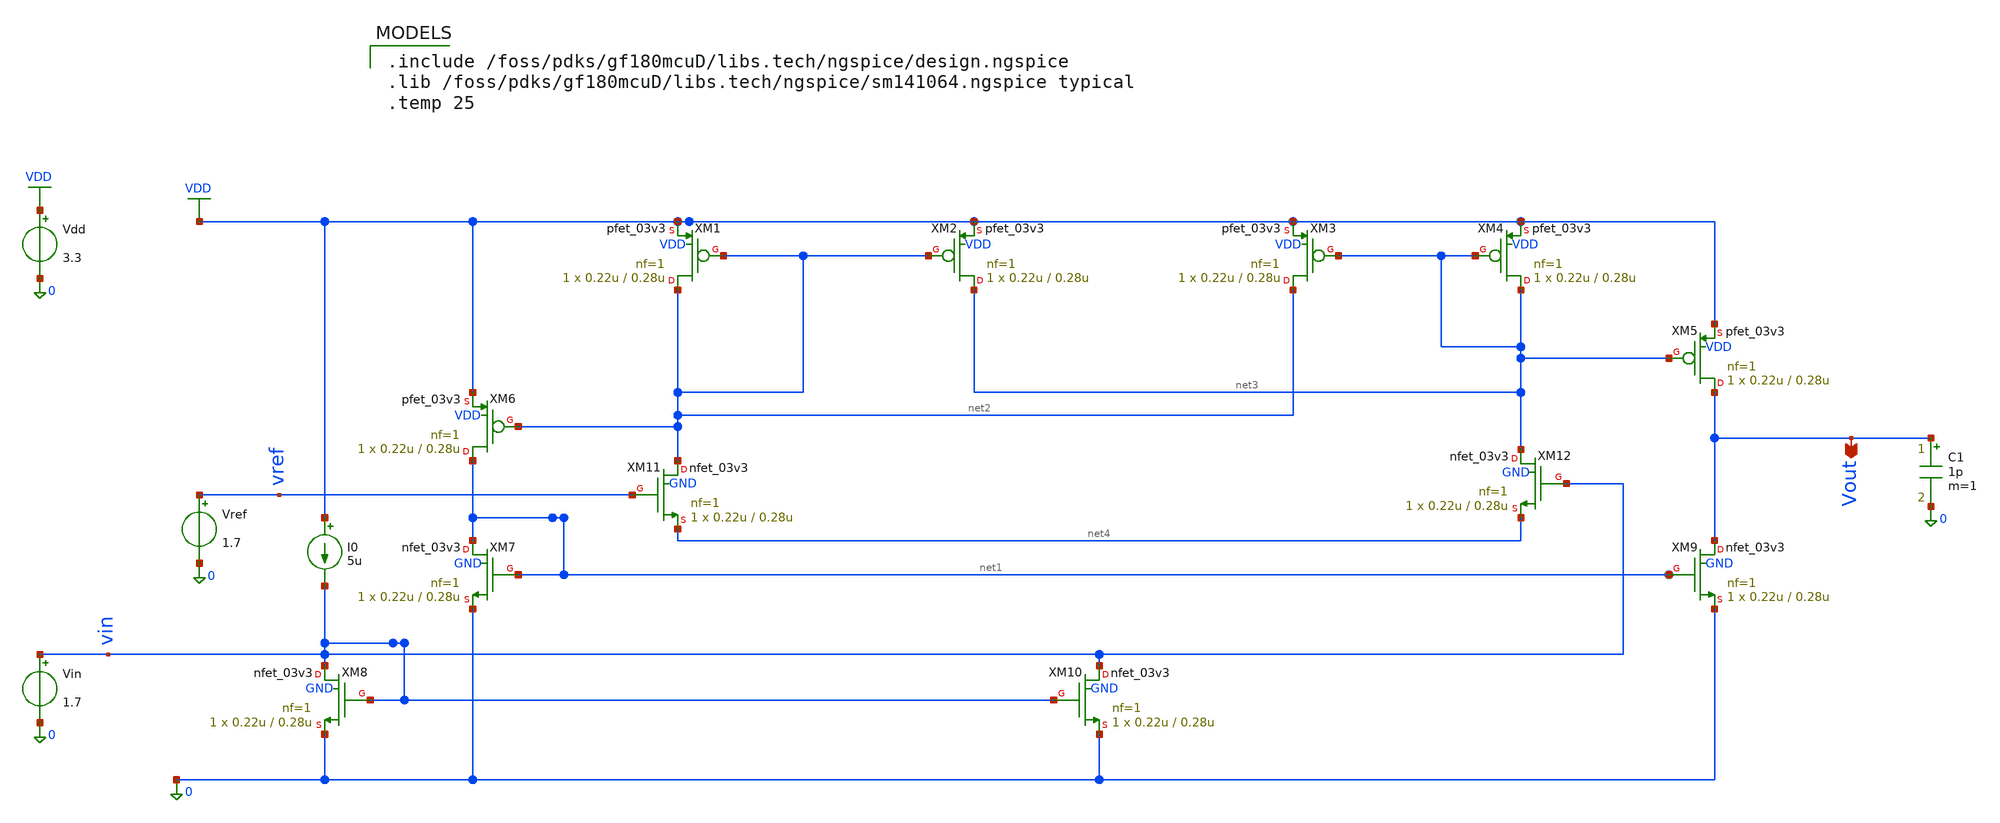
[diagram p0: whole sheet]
** sch_path: comparator/schematic-design/comparator_PVT.sch
**.subckt comparator_PVT Vout
*.opin Vout
XM1 net2 net2 VDD VDD pfet_03v3 L=0.28u W=0.22u nf=1 ad='int((nf+1)/2) * W/nf * 0.18u' as='int((nf+2)/2) * W/nf * 0.18u'
+ pd='2*int((nf+1)/2) * (W/nf + 0.18u)' ps='2*int((nf+2)/2) * (W/nf + 0.18u)' nrd='0.18u / W' nrs='0.18u / W'
+ sa=0 sb=0 sd=0 m=1 par=1
XM2 net3 net2 VDD VDD pfet_03v3 L=0.28u W=0.22u nf=1 ad='int((nf+1)/2) * W/nf * 0.18u' as='int((nf+2)/2) * W/nf * 0.18u'
+ pd='2*int((nf+1)/2) * (W/nf + 0.18u)' ps='2*int((nf+2)/2) * (W/nf + 0.18u)' nrd='0.18u / W' nrs='0.18u / W'
+ sa=0 sb=0 sd=0 m=1 par=1
XM3 net2 net3 VDD VDD pfet_03v3 L=0.28u W=0.22u nf=1 ad='int((nf+1)/2) * W/nf * 0.18u' as='int((nf+2)/2) * W/nf * 0.18u'
+ pd='2*int((nf+1)/2) * (W/nf + 0.18u)' ps='2*int((nf+2)/2) * (W/nf + 0.18u)' nrd='0.18u / W' nrs='0.18u / W'
+ sa=0 sb=0 sd=0 m=1 par=1
XM4 net3 net3 VDD VDD pfet_03v3 L=0.28u W=0.22u nf=1 ad='int((nf+1)/2) * W/nf * 0.18u' as='int((nf+2)/2) * W/nf * 0.18u'
+ pd='2*int((nf+1)/2) * (W/nf + 0.18u)' ps='2*int((nf+2)/2) * (W/nf + 0.18u)' nrd='0.18u / W' nrs='0.18u / W'
+ sa=0 sb=0 sd=0 m=1 par=1
XM5 Vout net3 VDD VDD pfet_03v3 L=0.28u W=0.22u nf=1 ad='int((nf+1)/2) * W/nf * 0.18u' as='int((nf+2)/2) * W/nf * 0.18u'
+ pd='2*int((nf+1)/2) * (W/nf + 0.18u)' ps='2*int((nf+2)/2) * (W/nf + 0.18u)' nrd='0.18u / W' nrs='0.18u / W'
+ sa=0 sb=0 sd=0 m=1 par=1
XM6 net1 net2 VDD VDD pfet_03v3 L=0.28u W=0.22u nf=1 ad='int((nf+1)/2) * W/nf * 0.18u' as='int((nf+2)/2) * W/nf * 0.18u'
+ pd='2*int((nf+1)/2) * (W/nf + 0.18u)' ps='2*int((nf+2)/2) * (W/nf + 0.18u)' nrd='0.18u / W' nrs='0.18u / W'
+ sa=0 sb=0 sd=0 m=1 par=1
XM7 net1 net1 0 GND nfet_03v3 L=0.28u W=0.22u nf=1 ad='int((nf+1)/2) * W/nf * 0.18u' as='int((nf+2)/2) * W/nf * 0.18u'
+ pd='2*int((nf+1)/2) * (W/nf + 0.18u)' ps='2*int((nf+2)/2) * (W/nf + 0.18u)' nrd='0.18u / W' nrs='0.18u / W'
+ sa=0 sb=0 sd=0 m=1 par=1
XM8 vin vin 0 GND nfet_03v3 L=0.28u W=0.22u nf=1 ad='int((nf+1)/2) * W/nf * 0.18u' as='int((nf+2)/2) * W/nf * 0.18u'
+ pd='2*int((nf+1)/2) * (W/nf + 0.18u)' ps='2*int((nf+2)/2) * (W/nf + 0.18u)' nrd='0.18u / W' nrs='0.18u / W'
+ sa=0 sb=0 sd=0 m=1 par=1
XM9 Vout net1 0 GND nfet_03v3 L=0.28u W=0.22u nf=1 ad='int((nf+1)/2) * W/nf * 0.18u' as='int((nf+2)/2) * W/nf * 0.18u'
+ pd='2*int((nf+1)/2) * (W/nf + 0.18u)' ps='2*int((nf+2)/2) * (W/nf + 0.18u)' nrd='0.18u / W' nrs='0.18u / W'
+ sa=0 sb=0 sd=0 m=1 par=1
XM10 vin vin 0 GND nfet_03v3 L=0.28u W=0.22u nf=1 ad='int((nf+1)/2) * W/nf * 0.18u' as='int((nf+2)/2) * W/nf * 0.18u'
+ pd='2*int((nf+1)/2) * (W/nf + 0.18u)' ps='2*int((nf+2)/2) * (W/nf + 0.18u)' nrd='0.18u / W' nrs='0.18u / W'
+ sa=0 sb=0 sd=0 m=1 par=1
XM11 net2 vref net4 GND nfet_03v3 L=0.28u W=0.22u nf=1 ad='int((nf+1)/2) * W/nf * 0.18u' as='int((nf+2)/2) * W/nf * 0.18u'
+ pd='2*int((nf+1)/2) * (W/nf + 0.18u)' ps='2*int((nf+2)/2) * (W/nf + 0.18u)' nrd='0.18u / W' nrs='0.18u / W'
+ sa=0 sb=0 sd=0 m=1 par=1
XM12 net3 vin net4 GND nfet_03v3 L=0.28u W=0.22u nf=1 ad='int((nf+1)/2) * W/nf * 0.18u' as='int((nf+2)/2) * W/nf * 0.18u'
+ pd='2*int((nf+1)/2) * (W/nf + 0.18u)' ps='2*int((nf+2)/2) * (W/nf + 0.18u)' nrd='0.18u / W' nrs='0.18u / W'
+ sa=0 sb=0 sd=0 m=1 par=1
I0 VDD vin 5u
Vref vref 0 1.7
Vin vin 0 1.7
Vdd VDD 0 3.3
C1 Vout 0 1p m=1
**** begin user architecture code

.include /foss/pdks/gf180mcuD/libs.tech/ngspice/design.ngspice
.lib /foss/pdks/gf180mcuD/libs.tech/ngspice/sm141064.ngspice typical
.temp 25


.control
set noaskquit
save all

tran 10n 120u

write comparator_pvt_tt.raw all

meas tran vout_high_tt max v(vout) from=5u to=120u
meas tran vout_low_tt min v(vout) from=5u to=120u

meas tran tpd_hl_tt trig v(vin) val=1.7 rise=1 targ v(vout) val=1.65 fall=1
meas tran tpd_lh_tt trig v(vin) val=1.7 fall=1 targ v(vout) val=1.65 rise=1

meas tran idd_avg_tt avg i(VDD) from=10u to=120u
let pavg_tt = abs(3.3 * idd_avg_tt)

print vout_high_tt
print vout_low_tt
print tpd_hl_tt
print tpd_lh_tt
print idd_avg_tt
print pavg_tt

.endc

**** end user architecture code
**.ends
.GLOBAL VDD
.end
